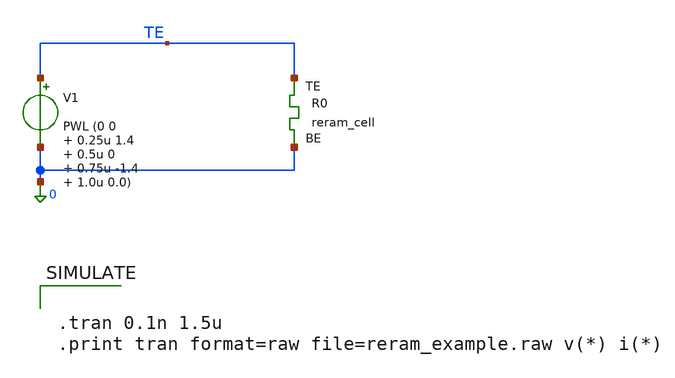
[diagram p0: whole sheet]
** sch_path: xschem/reram_examples/reram_example.sch
**.subckt reram_example
V1 TE 0 PWL (0 0 0.25u 1.4 0.5u 0 0.75u -1.4 1.0u 0.0)
XR0 TE 0 sky130_fd_pr_reram__reram_cell Tfilament_0=3.3e-9
**** begin user architecture code


.tran 0.1n 1.5u
.print tran format=raw file=reram_example.raw v(*) i(*)



** opencircuitdesign pdks install
.inc $::SKYWATER_MODELS/../xyce/sky130_fd_pr_reram__reram_cell.spice


**** end user architecture code
**.ends
.end
